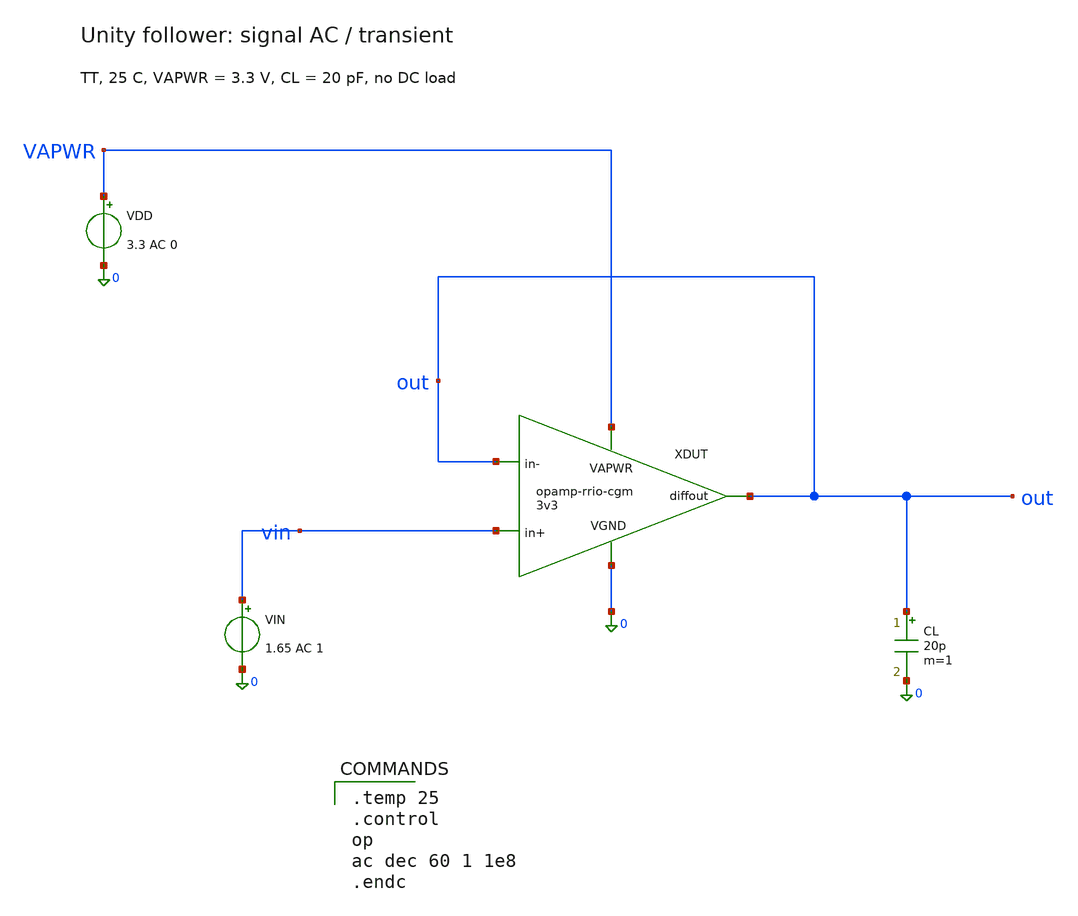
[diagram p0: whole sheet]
** sch_path: docs/simulation/xschem/bench-follower.sch
**.subckt bench-follower
XDUT VAPWR out vin out 0 opamp-rrio-cgm-3v3
VDD VAPWR 0 3.3 AC 0
VIN vin 0 1.65 AC 1
CL out 0 20p m=1
**** begin user architecture code
 .lib $::SKYWATER_MODELS/sky130.lib.spice tt

.temp 25
.control
op
ac dec 60 1 1e8
.endc

**** end user architecture code
**.ends
.end
